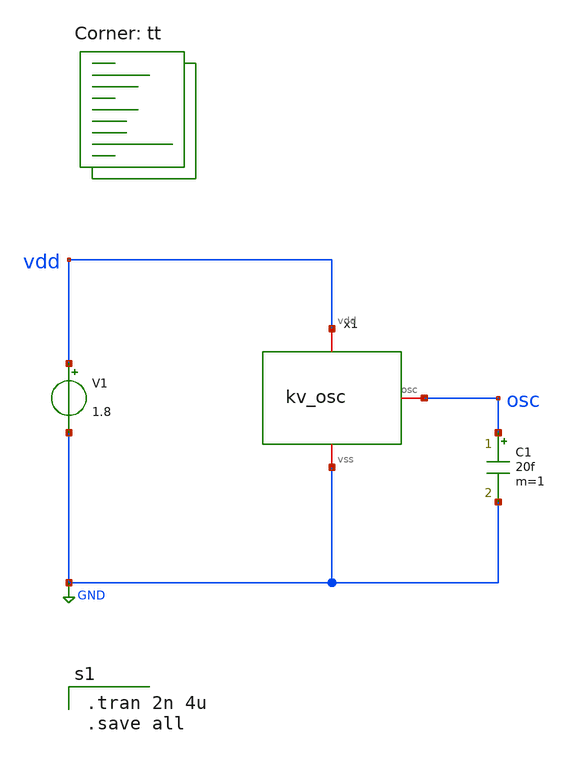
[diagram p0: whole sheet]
** sch_path: examples/demo_mixed/xschem/tb_osc.sch
**.subckt tb_osc
V1 vdd GND 1.8
x1 vdd GND osc kv_osc
C1 osc GND 20f m=1
**** begin user architecture code
.lib $::SKYWATER_MODELS/sky130.lib.spice tt

.tran 2n 4u
.save all

**** end user architecture code
**.ends
.GLOBAL GND
.end
